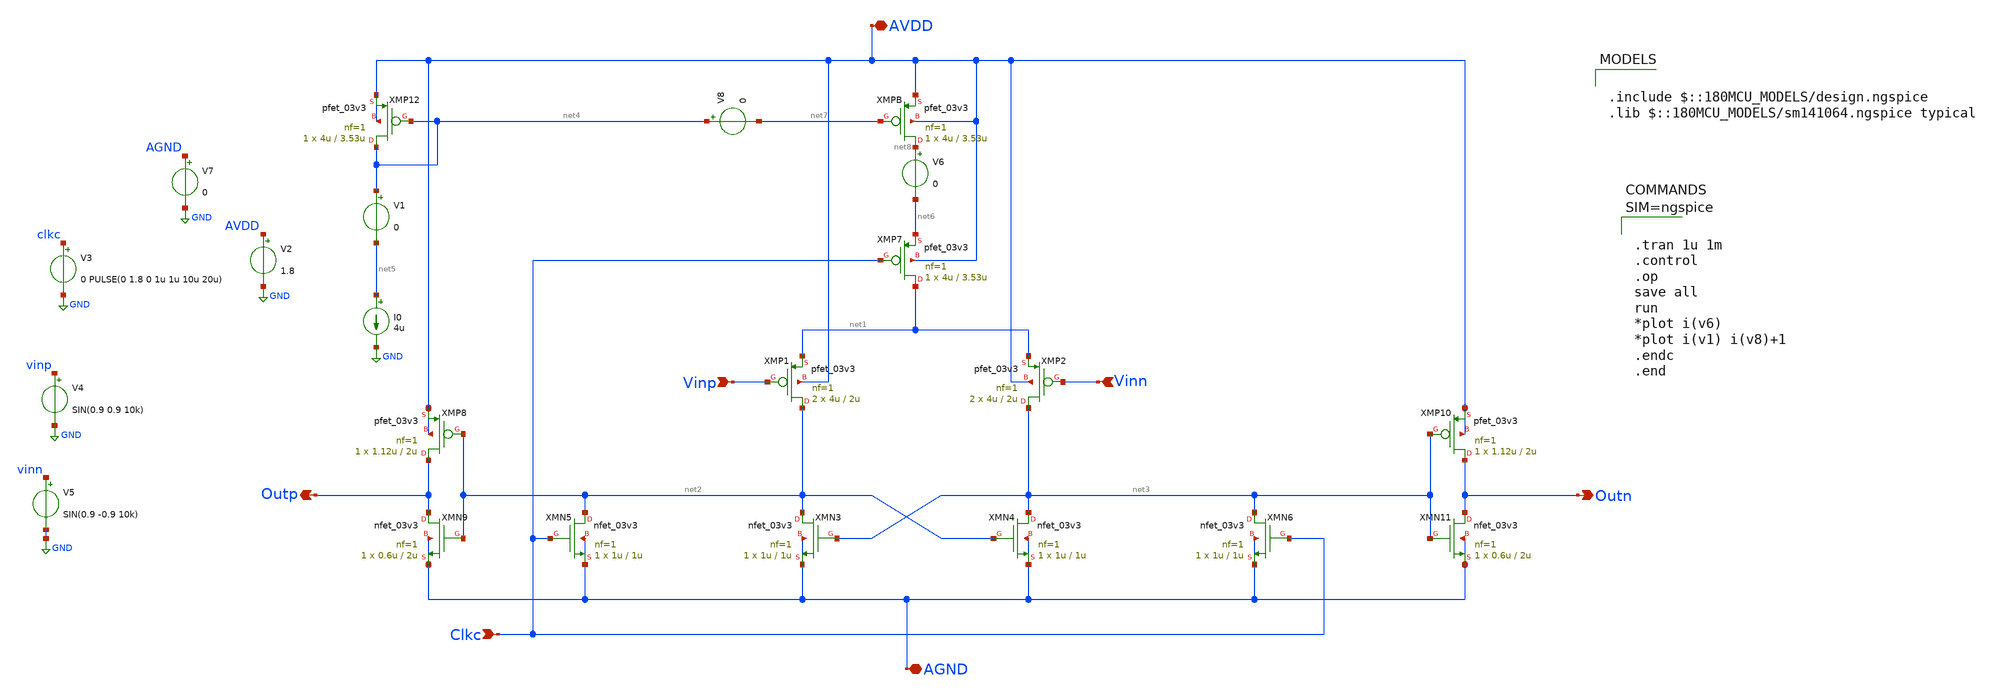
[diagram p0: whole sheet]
** sch_path: xschem/test_dyanamic_comp.sch
**.subckt test_dyanamic_comp AVDD Outp Clkc AGND Outn Vinp Vinn
*.iopin AVDD
*.opin Outp
*.ipin Clkc
*.iopin AGND
*.opin Outn
*.ipin Vinp
*.ipin Vinn
XMP1 net2 Vinp net1 AVDD pfet_03v3 L=2u W=4u nf=1 ad='int((nf+1)/2) * W/nf * 0.18u' as='int((nf+2)/2) * W/nf * 0.18u'
+ pd='2*int((nf+1)/2) * (W/nf + 0.18u)' ps='2*int((nf+2)/2) * (W/nf + 0.18u)' nrd='0.18u / W' nrs='0.18u / W'
+ sa=0 sb=0 sd=0 m=2
XMP2 net3 Vinn net1 AVDD pfet_03v3 L=2u W=4u nf=1 ad='int((nf+1)/2) * W/nf * 0.18u' as='int((nf+2)/2) * W/nf * 0.18u'
+ pd='2*int((nf+1)/2) * (W/nf + 0.18u)' ps='2*int((nf+2)/2) * (W/nf + 0.18u)' nrd='0.18u / W' nrs='0.18u / W'
+ sa=0 sb=0 sd=0 m=2
XMN4 net3 net2 AGND AGND nfet_03v3 L=1u W=1u nf=1 ad='int((nf+1)/2) * W/nf * 0.18u' as='int((nf+2)/2) * W/nf * 0.18u'
+ pd='2*int((nf+1)/2) * (W/nf + 0.18u)' ps='2*int((nf+2)/2) * (W/nf + 0.18u)' nrd='0.18u / W' nrs='0.18u / W'
+ sa=0 sb=0 sd=0 m=1
XMN5 net2 Clkc AGND AGND nfet_03v3 L=1u W=1u nf=1 ad='int((nf+1)/2) * W/nf * 0.18u' as='int((nf+2)/2) * W/nf * 0.18u'
+ pd='2*int((nf+1)/2) * (W/nf + 0.18u)' ps='2*int((nf+2)/2) * (W/nf + 0.18u)' nrd='0.18u / W' nrs='0.18u / W'
+ sa=0 sb=0 sd=0 m=1
XMN6 net3 Clkc AGND AGND nfet_03v3 L=1u W=1u nf=1 ad='int((nf+1)/2) * W/nf * 0.18u' as='int((nf+2)/2) * W/nf * 0.18u'
+ pd='2*int((nf+1)/2) * (W/nf + 0.18u)' ps='2*int((nf+2)/2) * (W/nf + 0.18u)' nrd='0.18u / W' nrs='0.18u / W'
+ sa=0 sb=0 sd=0 m=1
XMN3 net2 net3 AGND AGND nfet_03v3 L=1u W=1u nf=1 ad='int((nf+1)/2) * W/nf * 0.18u' as='int((nf+2)/2) * W/nf * 0.18u'
+ pd='2*int((nf+1)/2) * (W/nf + 0.18u)' ps='2*int((nf+2)/2) * (W/nf + 0.18u)' nrd='0.18u / W' nrs='0.18u / W'
+ sa=0 sb=0 sd=0 m=1
XMP7 net1 Clkc net6 AVDD pfet_03v3 L=3.53u W=4u nf=1 ad='int((nf+1)/2) * W/nf * 0.18u' as='int((nf+2)/2) * W/nf * 0.18u'
+ pd='2*int((nf+1)/2) * (W/nf + 0.18u)' ps='2*int((nf+2)/2) * (W/nf + 0.18u)' nrd='0.18u / W' nrs='0.18u / W'
+ sa=0 sb=0 sd=0 m=1
XMPB net8 net7 AVDD AVDD pfet_03v3 L=3.53u W=4u nf=1 ad='int((nf+1)/2) * W/nf * 0.18u' as='int((nf+2)/2) * W/nf * 0.18u'
+ pd='2*int((nf+1)/2) * (W/nf + 0.18u)' ps='2*int((nf+2)/2) * (W/nf + 0.18u)' nrd='0.18u / W' nrs='0.18u / W'
+ sa=0 sb=0 sd=0 m=1
XMP12 net4 net4 AVDD AVDD pfet_03v3 L=3.53u W=4u nf=1 ad='int((nf+1)/2) * W/nf * 0.18u' as='int((nf+2)/2) * W/nf * 0.18u'
+ pd='2*int((nf+1)/2) * (W/nf + 0.18u)' ps='2*int((nf+2)/2) * (W/nf + 0.18u)' nrd='0.18u / W' nrs='0.18u / W'
+ sa=0 sb=0 sd=0 m=1
XMP10 Outn net3 AVDD AVDD pfet_03v3 L=2u W=1.12u nf=1 ad='int((nf+1)/2) * W/nf * 0.18u' as='int((nf+2)/2) * W/nf * 0.18u'
+ pd='2*int((nf+1)/2) * (W/nf + 0.18u)' ps='2*int((nf+2)/2) * (W/nf + 0.18u)' nrd='0.18u / W' nrs='0.18u / W'
+ sa=0 sb=0 sd=0 m=1
XMN11 Outn net3 AGND AGND nfet_03v3 L=2u W=0.6u nf=1 ad='int((nf+1)/2) * W/nf * 0.18u' as='int((nf+2)/2) * W/nf * 0.18u'
+ pd='2*int((nf+1)/2) * (W/nf + 0.18u)' ps='2*int((nf+2)/2) * (W/nf + 0.18u)' nrd='0.18u / W' nrs='0.18u / W'
+ sa=0 sb=0 sd=0 m=1
XMP8 Outp net2 AVDD AVDD pfet_03v3 L=2u W=1.12u nf=1 ad='int((nf+1)/2) * W/nf * 0.18u' as='int((nf+2)/2) * W/nf * 0.18u'
+ pd='2*int((nf+1)/2) * (W/nf + 0.18u)' ps='2*int((nf+2)/2) * (W/nf + 0.18u)' nrd='0.18u / W' nrs='0.18u / W'
+ sa=0 sb=0 sd=0 m=1
XMN9 Outp net2 AGND AGND nfet_03v3 L=2u W=0.6u nf=1 ad='int((nf+1)/2) * W/nf * 0.18u' as='int((nf+2)/2) * W/nf * 0.18u'
+ pd='2*int((nf+1)/2) * (W/nf + 0.18u)' ps='2*int((nf+2)/2) * (W/nf + 0.18u)' nrd='0.18u / W' nrs='0.18u / W'
+ sa=0 sb=0 sd=0 m=1
V1 net4 net5 0
I0 net5 GND 4u
V2 AVDD GND 1.8
V3 clkc GND 0 PULSE(0 1.8 0 1u 1u 10u 20u)
V4 vinp GND SIN(0.9 0.9 10k)
V5 vinn GND SIN(0.9 -0.9 10k)
V6 net8 net6 0
V7 AGND GND 0
V8 net4 net7 0
**** begin user architecture code

.include $::180MCU_MODELS/design.ngspice
.lib $::180MCU_MODELS/sm141064.ngspice typical




.tran 1u 1m
.control
.op
save all
run
*plot i(v6)
*plot i(v1) i(v8)+1
.endc
.end



**** end user architecture code
**.ends
.GLOBAL GND
.end
